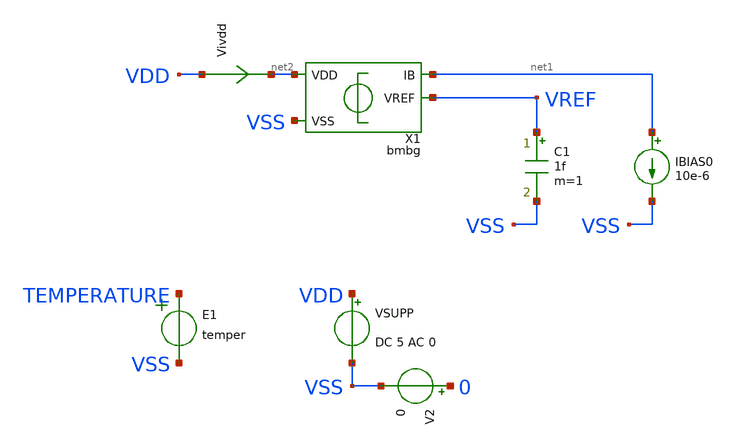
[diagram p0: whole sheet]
** sch_path: tt08/ip/bmbg/xschem/bmbg_tb.sch
**.subckt bmbg_tb
VSUPP VDD VSS DC 5 AC 0
V2 0 VSS 0
E1 TEMPERATURE VSS VOL=' temper '
IBIAS0 net1 VSS 10e-6
C1 VREF VSS 1f m=1
X1 net2 VSS net1 VREF bmbg
Vivdd VDD net2 0
.save i(vivdd)
**** begin user architecture code

.csparam TB_ID=$::TB_ID\
.csparam MC_RUNS=$::MC_RUNS\
.csparam EXIT_NGSPICE=$::EXIT_NGSPICE\
.lib $::SKYWATER_MODELS/sky130.lib.spice $::CORNER\


* this experimental option enables mos model bin
* selection based on W/NF instead of W
.option wnflag=0

.control
option savecurrents
save all

* dummy block for goto
if (1)
if TB_ID = 0
	goto TRAN_STARTUP
end
if TB_ID = 1
	goto TRAN_CURVE_TEMP
end
if TB_ID = 2
	goto VREF_NOISE
end
if TB_ID = 3
	goto AC_PSRR
end
if TB_ID = 4
	goto TRAN_CURVE_VDD
end
if TB_ID = 5
	goto TRAN_STARTUP
end

****************************************
label TRAN_CURVE_TEMP
save all
****************************************
if MC_RUNS = 0
	let veclen=3
	let vref_pp = vector(veclen)
	let vref_t20 = vector(veclen)
	let vref_tc20 = vector(veclen)
	let vref_mean = vector(veclen)
	let vsup = vector(veclen)
	let isup = vector(veclen)
	let run = 0

	foreach v_sweep 3 4 5
	*foreach v_sweep 3.3

		.include tran_curve_temp_ops.inc

		let run = run + 1
	end

	set nobreak
	set width=300
	print isup, vsup, vref_pp, vref_mean, vref_t20, vref_tc20 > dc.csv

else
	let vref_pp = vector(MC_RUNS)
	let vref_t20 = vector(MC_RUNS)
	let vref_tc20 = vector(MC_RUNS)
	let vref_mean = vector(MC_RUNS)
	let vsup = vector(MC_RUNS)
	let isup = vector(MC_RUNS)
	let run = 0
	set v_sweep = 5

	dowhile run < MC_RUNS
		echo MC-RUN: $&run

		.include tran_curve_temp_ops.inc

 		reset
		let run = run + 1
	end

	set nobreak
	set width=300
	print isup, vsup, vref_pp, vref_mean, vref_t20, vref_tc20 > dc.csv
end
goto done

****************************************
label TRAN_CURVE_VDD
save all
****************************************
if MC_RUNS = 0
	let veclen=3
	let vref_pp = vector(veclen)
	let vref_3v3 = vector(veclen)
	let vref_tc3v3 = vector(veclen)
	let vref_mean = vector(veclen)
	let te = vector(veclen)
	let isup = vector(veclen)
	let run = 0

	foreach t_sweep -40 20 140
	*foreach t_sweep 20

		.include tran_curve_vdd_ops.inc

		let run = run + 1
	end

	set nobreak
	set width=300
	print isup, te, vref_pp, vref_mean, vref_3v3, vref_tc3v3 > dc.csv

else
	let vref_pp = vector(MC_RUNS)
	let vref_3v3 = vector(MC_RUNS)
	let vref_tc3v3 = vector(MC_RUNS)
	let vref_mean = vector(MC_RUNS)
	let te = vector(MC_RUNS)
	let isup = vector(MC_RUNS)
	let run = 0
	set t_sweep = 20

	dowhile run < MC_RUNS
		echo MC-RUN: $&run

		.include tran_curve_vdd_ops.inc

 		reset
		let run = run + 1
	end

	set nobreak
	set width=300
	print isup, te, vref_pp, vref_mean, vref_3v3, vref_tc3v3 > dc.csv
end
goto done

****************************************
label VREF_NOISE
****************************************
noise v(vref) VSUPP dec 10 1 100e3 1
setplot noise2
print onoise_total
setplot noise1
plot onoise_spectrum
write noise1_isource.raw all

* https://sourceforge.net/p/ngspice/discussion/120973/thread/2aa3e30f/ -- Holger Vogt
* script to read a specific y-value if x given
**********************************************
let f0 = vector(1)
let f1 = vector(1)
let n_f0 = vector(1)
let n_f1 = vector(1)
compose freq_list values 10 10e3
foreach freq_idx 0 1
	let freq = freq_list[$freq_idx]
	* find index where freqency is just above interesting value
	setplot noise1
	let nn = 0
	while frequency[nn] < freq
		let nn = nn + 1
	end
	* define vectors of frequncies and values just above and below
	* selected frequeny
	let fnn = frequency[nn]
	let nn1 = nn - 1
	let fnn1 = frequency[nn1]
	let snn = onoise_spectrum[nn]
	let snn1 = onoise_spectrum[nn1]
	*print vector values
	echo nn = $&nn  fnn = $&fnn  snn = $&snn
	echo nn1 = $&nn1  fnn1 = $&fnn1  snn1 = $&snn1
	*linear interpolation for exact frequency
	let newsnn = snn1 + (snn - snn1)/(fnn - fnn1)*(freq - fnn1)
	echo newfnn = $&freq  newsnn = $&newsnn
	if $freq_idx = 0
		let f0 = freq
		let n_f0 = newsnn
	end
	if $freq_idx = 1
		let f1 = freq
		let n_f1 = newsnn
	end
end
set nobreak
set width=300
set noprintscale
print col f0, n_f0, f1, n_f1 > ac_inoise.csv

goto done

****************************************
label AC_PSRR
save all
****************************************
if MC_RUNS = 0
	let psrr_p_10Hz = vector(MC_RUNS+1)
	let psrr_p_10MHz = vector(MC_RUNS+1)
	let run=0

	.include ac_psrr_ops.inc

	set nobreak
	set width=300
	print col psrr_p_10Hz, psrr_p_10MHz > ac_psrr.csv
else
	let psrr_p_10Hz = vector(MC_RUNS)
	let psrr_p_10MHz = vector(MC_RUNS)
	let run=0
	dowhile run < MC_RUNS
		echo MC-RUN: $&run

		.include ac_psrr_ops.inc

 		reset
		let run = run + 1
	end
	set nobreak
	set width=300
	print psrr_p_10Hz, psrr_p_10MHz > ac_psrr.csv
end
goto done

****************************************
label TRAN_STARTUP
****************************************
if MC_RUNS = 0
	let veclen=4
	let startup_t = vector(veclen)
	let run=0
	foreach v_sweep 3 4 5 6
	*foreach v_sweep 3.3
		save all
		alter @VSUPP[pwl] = [ 0 0 100u $v_sweep]
		*alter @IBIAS0[pwl] = [ 0 0 100us 0 150us 10e-6 ]
  		tran 10n 200u
  		plot vivdd#branch
		plot VDD
		plot VREF
		meas tran m_vref_up when VREF=0.5 rise=1
		let startup_t[run] = m_vref_up
		write tran.raw all
		let run = run + 1
		set appendwrite
		reset
	end
	print startup_t > tran.csv
else
	let startup_t = vector(MC_RUNS)
	let run=0
	dowhile run < MC_RUNS
		echo MC-RUN: $&run
		alter @v1[pwl] = [ 0 0 1u 0 10u 3]
		tran 100n 20m
		meas tran m_cur_up when i(visource)=5e-6 rise=1
		let startup_t[run] = m_cur_up
 		reset
		let run = run + 1
	end
	print startup_t > tran.csv
end
goto done

****************************************
label done
****************************************
if EXIT_NGSPICE > 0.0
	exit
end
end
.endc


**** end user architecture code
**.ends

* expanding   symbol:  bmbg.sym # of pins=4
** sym_path: bmbg.sym
** sch_path: bmbg.sch
.subckt bmbg VDD VSS IB VREF
*.iopin VSS
*.iopin VDD
*.opin VREF
*.opin IB
XMSIT net3 vt VDD VDD sky130_fd_pr__pfet_g5v0d10v5 L=1 W=20 nf=1 ad='int((nf+1)/2) * W/nf * 0.29' as='int((nf+2)/2) * W/nf * 0.29'
+ pd='2*int((nf+1)/2) * (W/nf + 0.29)' ps='2*int((nf+2)/2) * (W/nf + 0.29)' nrd='0.29 / W' nrs='0.29 / W'
+ sa=0 sb=0 sd=0 mult=1 m=1
XQ1 VSS VSS vl sky130_fd_pr__pnp_05v5_W3p40L3p40 m=1
XQ2 VSS VSS net1 sky130_fd_pr__pnp_05v5_W3p40L3p40 m=1
X1 VDD VSS vt IB vl vr bmbgota
XMSIT1 net4 vt VDD VDD sky130_fd_pr__pfet_g5v0d10v5 L=1 W=20 nf=1 ad='int((nf+1)/2) * W/nf * 0.29' as='int((nf+2)/2) * W/nf * 0.29'
+ pd='2*int((nf+1)/2) * (W/nf + 0.29)' ps='2*int((nf+2)/2) * (W/nf + 0.29)' nrd='0.29 / W' nrs='0.29 / W'
+ sa=0 sb=0 sd=0 mult=1 m=1
XQ3 VSS VSS net2 sky130_fd_pr__pnp_05v5_W3p40L3p40 m=1
XMSIT2 VREF vt VDD VDD sky130_fd_pr__pfet_g5v0d10v5 L=1 W=20 nf=1 ad='int((nf+1)/2) * W/nf * 0.29' as='int((nf+2)/2) * W/nf * 0.29'
+ pd='2*int((nf+1)/2) * (W/nf + 0.29)' ps='2*int((nf+2)/2) * (W/nf + 0.29)' nrd='0.29 / W' nrs='0.29 / W'
+ sa=0 sb=0 sd=0 mult=1 m=1
XQ4 VSS VSS net1 sky130_fd_pr__pnp_05v5_W3p40L3p40 m=1
XQ5 VSS VSS net1 sky130_fd_pr__pnp_05v5_W3p40L3p40 m=1
XQ6 VSS VSS net1 sky130_fd_pr__pnp_05v5_W3p40L3p40 m=1
XQ7 VSS VSS net1 sky130_fd_pr__pnp_05v5_W3p40L3p40 m=1
XQ8 VSS VSS net1 sky130_fd_pr__pnp_05v5_W3p40L3p40 m=1
XQ9 VSS VSS net1 sky130_fd_pr__pnp_05v5_W3p40L3p40 m=1
XQ10 VSS VSS net1 sky130_fd_pr__pnp_05v5_W3p40L3p40 m=1
XRREF1 net2 VREF VSS sky130_fd_pr__res_xhigh_po_1p41 L=67 mult=1 m=1
XRREF2 net1 vr VSS sky130_fd_pr__res_xhigh_po_1p41 L=7 mult=1 m=1
XRSU VSS vsu VSS sky130_fd_pr__res_xhigh_po_0p69 L=203 mult=1 m=1
XMSIT3 vsu vt VDD VDD sky130_fd_pr__pfet_g5v0d10v5 L=1 W=20 nf=1 ad='int((nf+1)/2) * W/nf * 0.29' as='int((nf+2)/2) * W/nf * 0.29'
+ pd='2*int((nf+1)/2) * (W/nf + 0.29)' ps='2*int((nf+2)/2) * (W/nf + 0.29)' nrd='0.29 / W' nrs='0.29 / W'
+ sa=0 sb=0 sd=0 mult=5 m=5
XMSIT4 VSS vsu vt VDD sky130_fd_pr__pfet_g5v0d10v5 L=0.5 W=20 nf=1 ad='int((nf+1)/2) * W/nf * 0.29' as='int((nf+2)/2) * W/nf * 0.29'
+ pd='2*int((nf+1)/2) * (W/nf + 0.29)' ps='2*int((nf+2)/2) * (W/nf + 0.29)' nrd='0.29 / W' nrs='0.29 / W'
+ sa=0 sb=0 sd=0 mult=1 m=1
XRREF3 VSS VSS VSS sky130_fd_pr__res_xhigh_po_1p41 L=7 mult=1 m=1
XRREF4 VSS VSS VSS sky130_fd_pr__res_xhigh_po_1p41 L=7 mult=1 m=1
XRREF5 VSS VSS VSS sky130_fd_pr__res_xhigh_po_1p41 L=6.7 mult=1 m=1
XRREF6 VSS VSS VSS sky130_fd_pr__res_xhigh_po_1p41 L=6.7 mult=1 m=1
XMSIT5 VDD VDD VDD VDD sky130_fd_pr__pfet_g5v0d10v5 L=1 W=5 nf=1 ad='int((nf+1)/2) * W/nf * 0.29' as='int((nf+2)/2) * W/nf * 0.29'
+ pd='2*int((nf+1)/2) * (W/nf + 0.29)' ps='2*int((nf+2)/2) * (W/nf + 0.29)' nrd='0.29 / W' nrs='0.29 / W'
+ sa=0 sb=0 sd=0 mult=1 m=1
XMSIT6 VDD VDD VDD VDD sky130_fd_pr__pfet_g5v0d10v5 L=1 W=5 nf=1 ad='int((nf+1)/2) * W/nf * 0.29' as='int((nf+2)/2) * W/nf * 0.29'
+ pd='2*int((nf+1)/2) * (W/nf + 0.29)' ps='2*int((nf+2)/2) * (W/nf + 0.29)' nrd='0.29 / W' nrs='0.29 / W'
+ sa=0 sb=0 sd=0 mult=1 m=1
XRREF7 vr net4 VSS sky130_fd_pr__res_xhigh_po_1p41 L=21 mult=1 m=1
XRREF8 vl net3 VSS sky130_fd_pr__res_xhigh_po_1p41 L=21 mult=1 m=1
XRREF9 VSS VSS VSS sky130_fd_pr__res_xhigh_po_1p41 L=7 mult=1 m=1
XRREF10 VSS VSS VSS sky130_fd_pr__res_xhigh_po_1p41 L=7 mult=1 m=1
.ends


* expanding   symbol:  bmbgota.sym # of pins=6
** sym_path: bmbgota.sym
** sch_path: bmbgota.sch
.subckt bmbgota VDD VSS VOUT IB INN INP
*.iopin INP
*.iopin INN
*.iopin VOUT
*.opin IB
*.iopin VDD
*.iopin VSS
XMDR vr INP vt VDD sky130_fd_pr__pfet_g5v0d10v5 L=1 W=20 nf=1 ad='int((nf+1)/2) * W/nf * 0.29' as='int((nf+2)/2) * W/nf * 0.29'
+ pd='2*int((nf+1)/2) * (W/nf + 0.29)' ps='2*int((nf+2)/2) * (W/nf + 0.29)' nrd='0.29 / W' nrs='0.29 / W'
+ sa=0 sb=0 sd=0 mult=8 m=8
XMMIRL vl vl VSS VSS sky130_fd_pr__nfet_g5v0d10v5 L=2 W=5 nf=1 ad='int((nf+1)/2) * W/nf * 0.29' as='int((nf+2)/2) * W/nf * 0.29'
+ pd='2*int((nf+1)/2) * (W/nf + 0.29)' ps='2*int((nf+2)/2) * (W/nf + 0.29)' nrd='0.29 / W' nrs='0.29 / W'
+ sa=0 sb=0 sd=0 mult=4 m=4
XMMIRR vr vl VSS VSS sky130_fd_pr__nfet_g5v0d10v5 L=2 W=5 nf=1 ad='int((nf+1)/2) * W/nf * 0.29' as='int((nf+2)/2) * W/nf * 0.29'
+ pd='2*int((nf+1)/2) * (W/nf + 0.29)' ps='2*int((nf+2)/2) * (W/nf + 0.29)' nrd='0.29 / W' nrs='0.29 / W'
+ sa=0 sb=0 sd=0 mult=4 m=4
XMDL vl INN vt VDD sky130_fd_pr__pfet_g5v0d10v5 L=1 W=20 nf=1 ad='int((nf+1)/2) * W/nf * 0.29' as='int((nf+2)/2) * W/nf * 0.29'
+ pd='2*int((nf+1)/2) * (W/nf + 0.29)' ps='2*int((nf+2)/2) * (W/nf + 0.29)' nrd='0.29 / W' nrs='0.29 / W'
+ sa=0 sb=0 sd=0 mult=8 m=8
XMMIR2 vt IB VDD VDD sky130_fd_pr__pfet_g5v0d10v5 L=2 W=5 nf=1 ad='int((nf+1)/2) * W/nf * 0.29' as='int((nf+2)/2) * W/nf * 0.29'
+ pd='2*int((nf+1)/2) * (W/nf + 0.29)' ps='2*int((nf+2)/2) * (W/nf + 0.29)' nrd='0.29 / W' nrs='0.29 / W'
+ sa=0 sb=0 sd=0 mult=2 m=2
XMMIR1 IB IB VDD VDD sky130_fd_pr__pfet_g5v0d10v5 L=2 W=5 nf=1 ad='int((nf+1)/2) * W/nf * 0.29' as='int((nf+2)/2) * W/nf * 0.29'
+ pd='2*int((nf+1)/2) * (W/nf + 0.29)' ps='2*int((nf+2)/2) * (W/nf + 0.29)' nrd='0.29 / W' nrs='0.29 / W'
+ sa=0 sb=0 sd=0 mult=1 m=1
XMO VOUT vr VSS VSS sky130_fd_pr__nfet_g5v0d10v5 L=2 W=5 nf=1 ad='int((nf+1)/2) * W/nf * 0.29' as='int((nf+2)/2) * W/nf * 0.29'
+ pd='2*int((nf+1)/2) * (W/nf + 0.29)' ps='2*int((nf+2)/2) * (W/nf + 0.29)' nrd='0.29 / W' nrs='0.29 / W'
+ sa=0 sb=0 sd=0 mult=4 m=4
XMMIR3 VOUT IB VDD VDD sky130_fd_pr__pfet_g5v0d10v5 L=2 W=5 nf=1 ad='int((nf+1)/2) * W/nf * 0.29' as='int((nf+2)/2) * W/nf * 0.29'
+ pd='2*int((nf+1)/2) * (W/nf + 0.29)' ps='2*int((nf+2)/2) * (W/nf + 0.29)' nrd='0.29 / W' nrs='0.29 / W'
+ sa=0 sb=0 sd=0 mult=3 m=3
XR1 net1 vr VSS sky130_fd_pr__res_xhigh_po_1p41 L=7 mult=1 m=1
XC1 net1 VOUT sky130_fd_pr__cap_mim_m3_1 W=16 L=30 MF=1 m=1
XMDL1 VDD VDD VDD VDD sky130_fd_pr__pfet_g5v0d10v5 L=1 W=20 nf=1 ad='int((nf+1)/2) * W/nf * 0.29' as='int((nf+2)/2) * W/nf * 0.29'
+ pd='2*int((nf+1)/2) * (W/nf + 0.29)' ps='2*int((nf+2)/2) * (W/nf + 0.29)' nrd='0.29 / W' nrs='0.29 / W'
+ sa=0 sb=0 sd=0 mult=1 m=1
XMDR1 VDD VDD VDD VDD sky130_fd_pr__pfet_g5v0d10v5 L=1 W=20 nf=1 ad='int((nf+1)/2) * W/nf * 0.29' as='int((nf+2)/2) * W/nf * 0.29'
+ pd='2*int((nf+1)/2) * (W/nf + 0.29)' ps='2*int((nf+2)/2) * (W/nf + 0.29)' nrd='0.29 / W' nrs='0.29 / W'
+ sa=0 sb=0 sd=0 mult=1 m=1
XMMIRL1 VSS VSS VSS VSS sky130_fd_pr__nfet_g5v0d10v5 L=2 W=5 nf=1 ad='int((nf+1)/2) * W/nf * 0.29' as='int((nf+2)/2) * W/nf * 0.29'
+ pd='2*int((nf+1)/2) * (W/nf + 0.29)' ps='2*int((nf+2)/2) * (W/nf + 0.29)' nrd='0.29 / W' nrs='0.29 / W'
+ sa=0 sb=0 sd=0 mult=1 m=1
XMMIRR1 VSS VSS VSS VSS sky130_fd_pr__nfet_g5v0d10v5 L=2 W=5 nf=1 ad='int((nf+1)/2) * W/nf * 0.29' as='int((nf+2)/2) * W/nf * 0.29'
+ pd='2*int((nf+1)/2) * (W/nf + 0.29)' ps='2*int((nf+2)/2) * (W/nf + 0.29)' nrd='0.29 / W' nrs='0.29 / W'
+ sa=0 sb=0 sd=0 mult=1 m=1
.ends

.end
